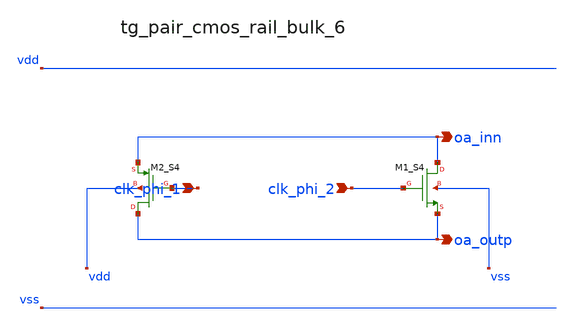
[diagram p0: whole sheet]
** sch_path: analog-db/raw/sup_003_rrl_sc_integrator/hier/blocks/tg_pair_cmos_rail_bulk_6.sch
**.subckt tg_pair_cmos_rail_bulk_6 clk_phi_1 clk_phi_2 oa_inn oa_outp
*.ipin clk_phi_1
*.ipin clk_phi_2
*.opin oa_inn
*.opin oa_outp
XM1_S4 oa_inn clk_phi_2 oa_outp vss sg13_lv_nmos w=x_dut_xm1_s4_w l=x_dut_xm1_s4_l ng=1
+ m=x_dut_xm1_s4_m
XM2_S4 oa_outp clk_phi_1 oa_inn vdd sg13_lv_pmos w=x_dut_xm2_s4_w l=x_dut_xm2_s4_l ng=1
+ m=x_dut_xm2_s4_m
**.ends
.end
